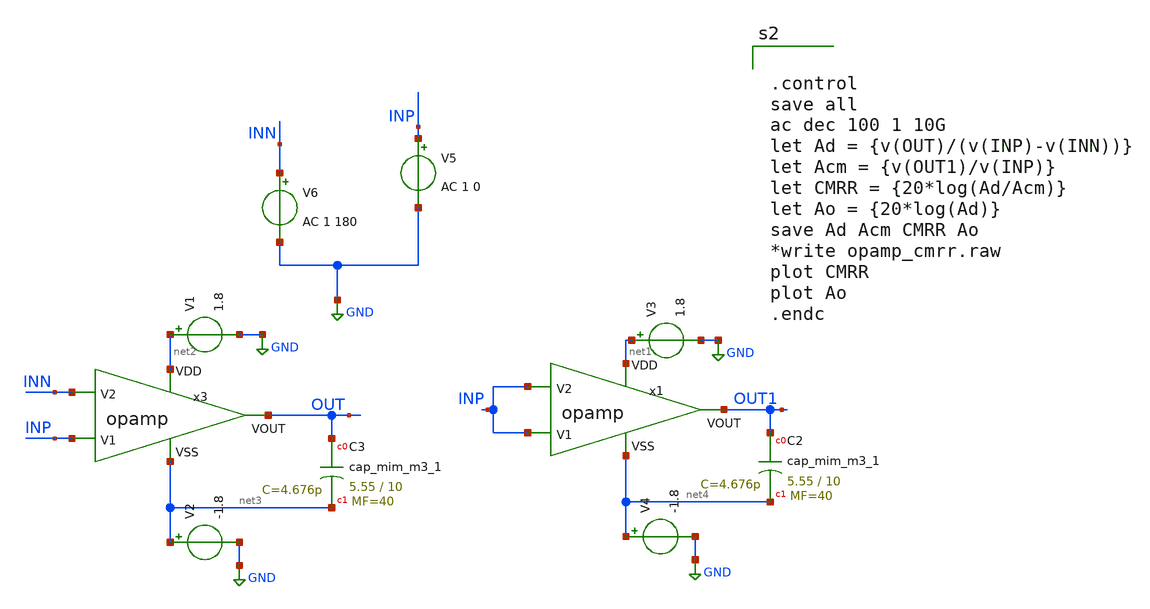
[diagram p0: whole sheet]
** sch_path: opamp_cmrr.sch
**.subckt opamp_cmrr
V6 INN GND AC 1 180
V5 INP GND AC 1 0
V1 net2 GND 1.8
V2 net3 GND -1.8
V3 net1 GND 1.8
V4 net4 GND -1.8
XC2 OUT1 net4 sky130_fd_pr__cap_mim_m3_1 W=5.55 L=10 MF=40 m=40
XC3 OUT net3 sky130_fd_pr__cap_mim_m3_1 W=5.55 L=10 MF=40 m=40
x3 net2 net3 INP INN OUT opamp
x1 net1 net4 INP INP OUT1 opamp
**** begin user architecture code


.control
save all
ac dec 100 1 10G
let Ad = {v(OUT)/(v(INP)-v(INN))}
let Acm = {v(OUT1)/v(INP)}
let CMRR = {20*log(Ad/Acm)}
let Ao = {20*log(Ad)}
save Ad Acm CMRR Ao
*write opamp_cmrr.raw
plot CMRR
plot Ao
.endc



** opencircuitdesign pdks install
.lib $::SKYWATER_MODELS/sky130.lib.spice tt


**** end user architecture code
**.ends

* expanding   symbol:  /foss/designs/chipalooza2024/sky130_hcmus_ip__instramp/opamp.sym # of pins=5
** sym_path: xschem/opamp.sym
** sch_path: xschem/opamp.sch
.subckt opamp VDD VSS V1 V2 VOUT
*.ipin VSS
*.ipin VDD
*.ipin V2
*.ipin V1
*.opin VOUT
XM2 net4 V2 net1 VSS sky130_fd_pr__nfet_g5v0d10v5 L=1 W=18 nf=1 ad='int((nf+1)/2) * W/nf * 0.29' as='int((nf+2)/2) * W/nf * 0.29'
+ pd='2*int((nf+1)/2) * (W/nf + 0.29)' ps='2*int((nf+2)/2) * (W/nf + 0.29)' nrd='0.29 / W' nrs='0.29 / W'
+ sa=0 sb=0 sd=0 mult=1 m=1
XM1 net5 net4 VDD VDD sky130_fd_pr__pfet_g5v0d10v5 L=1 W=30 nf=1 ad='int((nf+1)/2) * W/nf * 0.29' as='int((nf+2)/2) * W/nf * 0.29'
+ pd='2*int((nf+1)/2) * (W/nf + 0.29)' ps='2*int((nf+2)/2) * (W/nf + 0.29)' nrd='0.29 / W' nrs='0.29 / W'
+ sa=0 sb=0 sd=0 mult=1 m=1
XM4 net5 V1 net1 VSS sky130_fd_pr__nfet_g5v0d10v5 L=1 W=18 nf=1 ad='int((nf+1)/2) * W/nf * 0.29' as='int((nf+2)/2) * W/nf * 0.29'
+ pd='2*int((nf+1)/2) * (W/nf + 0.29)' ps='2*int((nf+2)/2) * (W/nf + 0.29)' nrd='0.29 / W' nrs='0.29 / W'
+ sa=0 sb=0 sd=0 mult=1 m=1
XM5 net1 net6 VSS VSS sky130_fd_pr__nfet_g5v0d10v5 L=1 W=15.171 nf=1 ad='int((nf+1)/2) * W/nf * 0.29'
+ as='int((nf+2)/2) * W/nf * 0.29' pd='2*int((nf+1)/2) * (W/nf + 0.29)' ps='2*int((nf+2)/2) * (W/nf + 0.29)'
+ nrd='0.29 / W' nrs='0.29 / W' sa=0 sb=0 sd=0 mult=1 m=1
XM6 VOUT net6 VSS VSS sky130_fd_pr__nfet_g5v0d10v5 L=1 W=19 nf=1 ad='int((nf+1)/2) * W/nf * 0.29' as='int((nf+2)/2) * W/nf * 0.29'
+ pd='2*int((nf+1)/2) * (W/nf + 0.29)' ps='2*int((nf+2)/2) * (W/nf + 0.29)' nrd='0.29 / W' nrs='0.29 / W'
+ sa=0 sb=0 sd=0 mult=1 m=1
XM7 net6 net6 VSS VSS sky130_fd_pr__nfet_g5v0d10v5 L=1 W=20 nf=1 ad='int((nf+1)/2) * W/nf * 0.29' as='int((nf+2)/2) * W/nf * 0.29'
+ pd='2*int((nf+1)/2) * (W/nf + 0.29)' ps='2*int((nf+2)/2) * (W/nf + 0.29)' nrd='0.29 / W' nrs='0.29 / W'
+ sa=0 sb=0 sd=0 mult=1 m=1
XM3 net4 net4 VDD VDD sky130_fd_pr__pfet_g5v0d10v5 L=1 W=30 nf=1 ad='int((nf+1)/2) * W/nf * 0.29' as='int((nf+2)/2) * W/nf * 0.29'
+ pd='2*int((nf+1)/2) * (W/nf + 0.29)' ps='2*int((nf+2)/2) * (W/nf + 0.29)' nrd='0.29 / W' nrs='0.29 / W'
+ sa=0 sb=0 sd=0 mult=1 m=1
XM8 VOUT net5 VDD VDD sky130_fd_pr__pfet_g5v0d10v5 L=1 W=38 nf=1 ad='int((nf+1)/2) * W/nf * 0.29' as='int((nf+2)/2) * W/nf * 0.29'
+ pd='2*int((nf+1)/2) * (W/nf + 0.29)' ps='2*int((nf+2)/2) * (W/nf + 0.29)' nrd='0.29 / W' nrs='0.29 / W'
+ sa=0 sb=0 sd=0 mult=2 m=2
XC1 net7 net5 sky130_fd_pr__cap_mim_m3_1 W=5.5 L=10 MF=10 m=10
V_ibias net8 net6 0
.save i(v_ibias)
XR5 net2 VDD VSS sky130_fd_pr__res_high_po_0p69 L=18.58 mult=1 m=1
XR1 net3 net2 VSS sky130_fd_pr__res_high_po_0p69 L=18.58 mult=1 m=1
XR2 net8 net3 VSS sky130_fd_pr__res_high_po_0p69 L=18.58 mult=1 m=1
XR3 net7 VOUT VSS sky130_fd_pr__res_high_po_0p69 L=2.41 mult=1 m=1
.ends

.GLOBAL GND
.end
